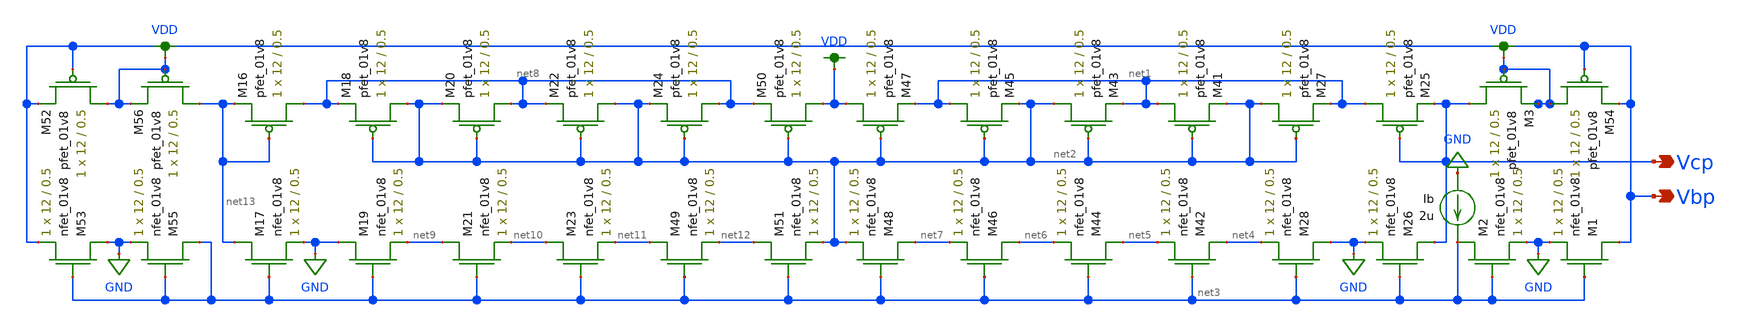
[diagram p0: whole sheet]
** sch_path: simulation/dac/v_gen_lds.sch
**.subckt v_gen_lds Vcp Vbp
*.opin Vcp
*.opin Vbp
XM25 net1 Vcp Vcp VDD sky130_fd_pr__pfet_01v8 L=0.5 W=12 nf=1 ad='int((nf+1)/2) * W/nf * 0.29' as='int((nf+2)/2) * W/nf * 0.29'
+ pd='2*int((nf+1)/2) * (W/nf + 0.29)' ps='2*int((nf+2)/2) * (W/nf + 0.29)' nrd='0.29 / W' nrs='0.29 / W'
+ sa=0 sb=0 sd=0 mult=1 m=1
XM26 Vcp net3 GND GND sky130_fd_pr__nfet_01v8 L=0.5 W=12 nf=1 ad='int((nf+1)/2) * W/nf * 0.29' as='int((nf+2)/2) * W/nf * 0.29'
+ pd='2*int((nf+1)/2) * (W/nf + 0.29)' ps='2*int((nf+2)/2) * (W/nf + 0.29)' nrd='0.29 / W' nrs='0.29 / W'
+ sa=0 sb=0 sd=0 mult=1 m=1
XM27 net2 net2 net1 VDD sky130_fd_pr__pfet_01v8 L=0.5 W=12 nf=1 ad='int((nf+1)/2) * W/nf * 0.29' as='int((nf+2)/2) * W/nf * 0.29'
+ pd='2*int((nf+1)/2) * (W/nf + 0.29)' ps='2*int((nf+2)/2) * (W/nf + 0.29)' nrd='0.29 / W' nrs='0.29 / W'
+ sa=0 sb=0 sd=0 mult=1 m=1
XM28 GND net3 net4 GND sky130_fd_pr__nfet_01v8 L=0.5 W=12 nf=1 ad='int((nf+1)/2) * W/nf * 0.29' as='int((nf+2)/2) * W/nf * 0.29'
+ pd='2*int((nf+1)/2) * (W/nf + 0.29)' ps='2*int((nf+2)/2) * (W/nf + 0.29)' nrd='0.29 / W' nrs='0.29 / W'
+ sa=0 sb=0 sd=0 mult=1 m=1
XM41 net1 net2 net2 VDD sky130_fd_pr__pfet_01v8 L=0.5 W=12 nf=1 ad='int((nf+1)/2) * W/nf * 0.29' as='int((nf+2)/2) * W/nf * 0.29'
+ pd='2*int((nf+1)/2) * (W/nf + 0.29)' ps='2*int((nf+2)/2) * (W/nf + 0.29)' nrd='0.29 / W' nrs='0.29 / W'
+ sa=0 sb=0 sd=0 mult=1 m=1
XM42 net4 net3 net5 GND sky130_fd_pr__nfet_01v8 L=0.5 W=12 nf=1 ad='int((nf+1)/2) * W/nf * 0.29' as='int((nf+2)/2) * W/nf * 0.29'
+ pd='2*int((nf+1)/2) * (W/nf + 0.29)' ps='2*int((nf+2)/2) * (W/nf + 0.29)' nrd='0.29 / W' nrs='0.29 / W'
+ sa=0 sb=0 sd=0 mult=1 m=1
XM43 net2 net2 net1 VDD sky130_fd_pr__pfet_01v8 L=0.5 W=12 nf=1 ad='int((nf+1)/2) * W/nf * 0.29' as='int((nf+2)/2) * W/nf * 0.29'
+ pd='2*int((nf+1)/2) * (W/nf + 0.29)' ps='2*int((nf+2)/2) * (W/nf + 0.29)' nrd='0.29 / W' nrs='0.29 / W'
+ sa=0 sb=0 sd=0 mult=1 m=1
XM44 net5 net3 net6 GND sky130_fd_pr__nfet_01v8 L=0.5 W=12 nf=1 ad='int((nf+1)/2) * W/nf * 0.29' as='int((nf+2)/2) * W/nf * 0.29'
+ pd='2*int((nf+1)/2) * (W/nf + 0.29)' ps='2*int((nf+2)/2) * (W/nf + 0.29)' nrd='0.29 / W' nrs='0.29 / W'
+ sa=0 sb=0 sd=0 mult=1 m=1
XM45 net1 net2 net2 VDD sky130_fd_pr__pfet_01v8 L=0.5 W=12 nf=1 ad='int((nf+1)/2) * W/nf * 0.29' as='int((nf+2)/2) * W/nf * 0.29'
+ pd='2*int((nf+1)/2) * (W/nf + 0.29)' ps='2*int((nf+2)/2) * (W/nf + 0.29)' nrd='0.29 / W' nrs='0.29 / W'
+ sa=0 sb=0 sd=0 mult=1 m=1
XM46 net6 net3 net7 GND sky130_fd_pr__nfet_01v8 L=0.5 W=12 nf=1 ad='int((nf+1)/2) * W/nf * 0.29' as='int((nf+2)/2) * W/nf * 0.29'
+ pd='2*int((nf+1)/2) * (W/nf + 0.29)' ps='2*int((nf+2)/2) * (W/nf + 0.29)' nrd='0.29 / W' nrs='0.29 / W'
+ sa=0 sb=0 sd=0 mult=1 m=1
XM47 VDD net2 net1 VDD sky130_fd_pr__pfet_01v8 L=0.5 W=12 nf=1 ad='int((nf+1)/2) * W/nf * 0.29' as='int((nf+2)/2) * W/nf * 0.29'
+ pd='2*int((nf+1)/2) * (W/nf + 0.29)' ps='2*int((nf+2)/2) * (W/nf + 0.29)' nrd='0.29 / W' nrs='0.29 / W'
+ sa=0 sb=0 sd=0 mult=1 m=1
XM48 net7 net3 net2 GND sky130_fd_pr__nfet_01v8 L=0.5 W=12 nf=1 ad='int((nf+1)/2) * W/nf * 0.29' as='int((nf+2)/2) * W/nf * 0.29'
+ pd='2*int((nf+1)/2) * (W/nf + 0.29)' ps='2*int((nf+2)/2) * (W/nf + 0.29)' nrd='0.29 / W' nrs='0.29 / W'
+ sa=0 sb=0 sd=0 mult=1 m=1
XM54 VDD Vbp Vbp VDD sky130_fd_pr__pfet_01v8 L=0.5 W=12 nf=1 ad='int((nf+1)/2) * W/nf * 0.29' as='int((nf+2)/2) * W/nf * 0.29'
+ pd='2*int((nf+1)/2) * (W/nf + 0.29)' ps='2*int((nf+2)/2) * (W/nf + 0.29)' nrd='0.29 / W' nrs='0.29 / W'
+ sa=0 sb=0 sd=0 mult=1 m=1
XM1 Vbp net3 GND GND sky130_fd_pr__nfet_01v8 L=0.5 W=12 nf=1 ad='int((nf+1)/2) * W/nf * 0.29' as='int((nf+2)/2) * W/nf * 0.29'
+ pd='2*int((nf+1)/2) * (W/nf + 0.29)' ps='2*int((nf+2)/2) * (W/nf + 0.29)' nrd='0.29 / W' nrs='0.29 / W'
+ sa=0 sb=0 sd=0 mult=1 m=1
XM2 net3 net3 GND GND sky130_fd_pr__nfet_01v8 L=0.5 W=12 nf=1 ad='int((nf+1)/2) * W/nf * 0.29' as='int((nf+2)/2) * W/nf * 0.29'
+ pd='2*int((nf+1)/2) * (W/nf + 0.29)' ps='2*int((nf+2)/2) * (W/nf + 0.29)' nrd='0.29 / W' nrs='0.29 / W'
+ sa=0 sb=0 sd=0 mult=1 m=1
XM3 Vcp VDD VDD VDD sky130_fd_pr__pfet_01v8 L=0.5 W=12 nf=1 ad='int((nf+1)/2) * W/nf * 0.29' as='int((nf+2)/2) * W/nf * 0.29'
+ pd='2*int((nf+1)/2) * (W/nf + 0.29)' ps='2*int((nf+2)/2) * (W/nf + 0.29)' nrd='0.29 / W' nrs='0.29 / W'
+ sa=0 sb=0 sd=0 mult=1 m=1
XM16 net8 net13 net13 VDD sky130_fd_pr__pfet_01v8 L=0.5 W=12 nf=1 ad='int((nf+1)/2) * W/nf * 0.29' as='int((nf+2)/2) * W/nf * 0.29'
+ pd='2*int((nf+1)/2) * (W/nf + 0.29)' ps='2*int((nf+2)/2) * (W/nf + 0.29)' nrd='0.29 / W' nrs='0.29 / W'
+ sa=0 sb=0 sd=0 mult=1 m=1
XM17 net13 net3 GND GND sky130_fd_pr__nfet_01v8 L=0.5 W=12 nf=1 ad='int((nf+1)/2) * W/nf * 0.29' as='int((nf+2)/2) * W/nf * 0.29'
+ pd='2*int((nf+1)/2) * (W/nf + 0.29)' ps='2*int((nf+2)/2) * (W/nf + 0.29)' nrd='0.29 / W' nrs='0.29 / W'
+ sa=0 sb=0 sd=0 mult=1 m=1
XM18 net2 net2 net8 VDD sky130_fd_pr__pfet_01v8 L=0.5 W=12 nf=1 ad='int((nf+1)/2) * W/nf * 0.29' as='int((nf+2)/2) * W/nf * 0.29'
+ pd='2*int((nf+1)/2) * (W/nf + 0.29)' ps='2*int((nf+2)/2) * (W/nf + 0.29)' nrd='0.29 / W' nrs='0.29 / W'
+ sa=0 sb=0 sd=0 mult=1 m=1
XM19 GND net3 net9 GND sky130_fd_pr__nfet_01v8 L=0.5 W=12 nf=1 ad='int((nf+1)/2) * W/nf * 0.29' as='int((nf+2)/2) * W/nf * 0.29'
+ pd='2*int((nf+1)/2) * (W/nf + 0.29)' ps='2*int((nf+2)/2) * (W/nf + 0.29)' nrd='0.29 / W' nrs='0.29 / W'
+ sa=0 sb=0 sd=0 mult=1 m=1
XM20 net8 net2 net2 VDD sky130_fd_pr__pfet_01v8 L=0.5 W=12 nf=1 ad='int((nf+1)/2) * W/nf * 0.29' as='int((nf+2)/2) * W/nf * 0.29'
+ pd='2*int((nf+1)/2) * (W/nf + 0.29)' ps='2*int((nf+2)/2) * (W/nf + 0.29)' nrd='0.29 / W' nrs='0.29 / W'
+ sa=0 sb=0 sd=0 mult=1 m=1
XM21 net9 net3 net10 GND sky130_fd_pr__nfet_01v8 L=0.5 W=12 nf=1 ad='int((nf+1)/2) * W/nf * 0.29' as='int((nf+2)/2) * W/nf * 0.29'
+ pd='2*int((nf+1)/2) * (W/nf + 0.29)' ps='2*int((nf+2)/2) * (W/nf + 0.29)' nrd='0.29 / W' nrs='0.29 / W'
+ sa=0 sb=0 sd=0 mult=1 m=1
XM22 net2 net2 net8 VDD sky130_fd_pr__pfet_01v8 L=0.5 W=12 nf=1 ad='int((nf+1)/2) * W/nf * 0.29' as='int((nf+2)/2) * W/nf * 0.29'
+ pd='2*int((nf+1)/2) * (W/nf + 0.29)' ps='2*int((nf+2)/2) * (W/nf + 0.29)' nrd='0.29 / W' nrs='0.29 / W'
+ sa=0 sb=0 sd=0 mult=1 m=1
XM23 net10 net3 net11 GND sky130_fd_pr__nfet_01v8 L=0.5 W=12 nf=1 ad='int((nf+1)/2) * W/nf * 0.29' as='int((nf+2)/2) * W/nf * 0.29'
+ pd='2*int((nf+1)/2) * (W/nf + 0.29)' ps='2*int((nf+2)/2) * (W/nf + 0.29)' nrd='0.29 / W' nrs='0.29 / W'
+ sa=0 sb=0 sd=0 mult=1 m=1
XM24 net8 net2 net2 VDD sky130_fd_pr__pfet_01v8 L=0.5 W=12 nf=1 ad='int((nf+1)/2) * W/nf * 0.29' as='int((nf+2)/2) * W/nf * 0.29'
+ pd='2*int((nf+1)/2) * (W/nf + 0.29)' ps='2*int((nf+2)/2) * (W/nf + 0.29)' nrd='0.29 / W' nrs='0.29 / W'
+ sa=0 sb=0 sd=0 mult=1 m=1
XM49 net11 net3 net12 GND sky130_fd_pr__nfet_01v8 L=0.5 W=12 nf=1 ad='int((nf+1)/2) * W/nf * 0.29' as='int((nf+2)/2) * W/nf * 0.29'
+ pd='2*int((nf+1)/2) * (W/nf + 0.29)' ps='2*int((nf+2)/2) * (W/nf + 0.29)' nrd='0.29 / W' nrs='0.29 / W'
+ sa=0 sb=0 sd=0 mult=1 m=1
XM50 VDD net2 net8 VDD sky130_fd_pr__pfet_01v8 L=0.5 W=12 nf=1 ad='int((nf+1)/2) * W/nf * 0.29' as='int((nf+2)/2) * W/nf * 0.29'
+ pd='2*int((nf+1)/2) * (W/nf + 0.29)' ps='2*int((nf+2)/2) * (W/nf + 0.29)' nrd='0.29 / W' nrs='0.29 / W'
+ sa=0 sb=0 sd=0 mult=1 m=1
XM51 net12 net3 net2 GND sky130_fd_pr__nfet_01v8 L=0.5 W=12 nf=1 ad='int((nf+1)/2) * W/nf * 0.29' as='int((nf+2)/2) * W/nf * 0.29'
+ pd='2*int((nf+1)/2) * (W/nf + 0.29)' ps='2*int((nf+2)/2) * (W/nf + 0.29)' nrd='0.29 / W' nrs='0.29 / W'
+ sa=0 sb=0 sd=0 mult=1 m=1
XM52 VDD Vbp Vbp VDD sky130_fd_pr__pfet_01v8 L=0.5 W=12 nf=1 ad='int((nf+1)/2) * W/nf * 0.29' as='int((nf+2)/2) * W/nf * 0.29'
+ pd='2*int((nf+1)/2) * (W/nf + 0.29)' ps='2*int((nf+2)/2) * (W/nf + 0.29)' nrd='0.29 / W' nrs='0.29 / W'
+ sa=0 sb=0 sd=0 mult=1 m=1
XM53 GND net3 Vbp GND sky130_fd_pr__nfet_01v8 L=0.5 W=12 nf=1 ad='int((nf+1)/2) * W/nf * 0.29' as='int((nf+2)/2) * W/nf * 0.29'
+ pd='2*int((nf+1)/2) * (W/nf + 0.29)' ps='2*int((nf+2)/2) * (W/nf + 0.29)' nrd='0.29 / W' nrs='0.29 / W'
+ sa=0 sb=0 sd=0 mult=1 m=1
XM55 net3 net3 GND GND sky130_fd_pr__nfet_01v8 L=0.5 W=12 nf=1 ad='int((nf+1)/2) * W/nf * 0.29' as='int((nf+2)/2) * W/nf * 0.29'
+ pd='2*int((nf+1)/2) * (W/nf + 0.29)' ps='2*int((nf+2)/2) * (W/nf + 0.29)' nrd='0.29 / W' nrs='0.29 / W'
+ sa=0 sb=0 sd=0 mult=1 m=1
XM56 net13 VDD VDD VDD sky130_fd_pr__pfet_01v8 L=0.5 W=12 nf=1 ad='int((nf+1)/2) * W/nf * 0.29' as='int((nf+2)/2) * W/nf * 0.29'
+ pd='2*int((nf+1)/2) * (W/nf + 0.29)' ps='2*int((nf+2)/2) * (W/nf + 0.29)' nrd='0.29 / W' nrs='0.29 / W'
+ sa=0 sb=0 sd=0 mult=1 m=1
Ib GND net3 2u
**.ends
.GLOBAL GND
.GLOBAL VDD
.end
